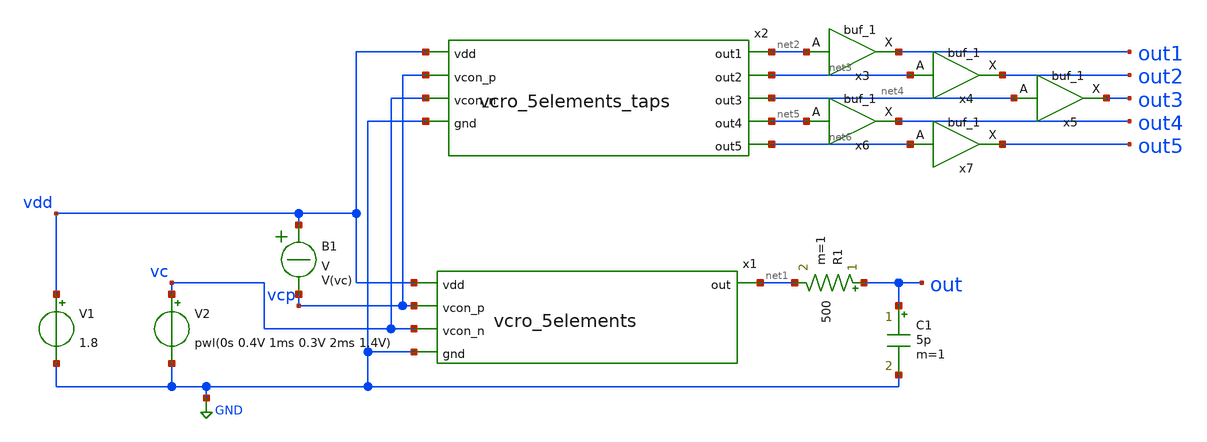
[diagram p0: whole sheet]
** sch_path: xschem/vcro_5st_tb.sch
**.subckt vcro_5st_tb
V1 vdd GND 1.8
V2 vc GND pwl(0s 0.4V 1ms 0.3V 2ms 1.4V)
R1 out net1 500 m=1
B1 vdd vcp V = V(vc)
x1 net1 vdd vcp vc GND vcro_5elements
C1 out GND 5p m=1
x2 net2 net3 net4 net5 net6 vdd vcp vc GND vcro_5elements_taps
x3 net2 GND GND vdd vdd out1 sky130_fd_sc_hd__buf_1
x4 net3 GND GND vdd vdd out2 sky130_fd_sc_hd__buf_1
x5 net4 GND GND vdd vdd out3 sky130_fd_sc_hd__buf_1
x6 net5 GND GND vdd vdd out4 sky130_fd_sc_hd__buf_1
x7 net6 GND GND vdd vdd out5 sky130_fd_sc_hd__buf_1
**** begin user architecture code
 .lib $::SKYWATER_MODELS/sky130.lib.spice tt
.include $::SKYWATER_STDCELLS/../../sky130_fd_sc_hd/spice/sky130_fd_sc_hd.spice

.param mc_mm_switch=0
.param mc_pr_switch=1



.option wnflag=0
.option savecurrents
.control
save all
tran 10n 2m 1m
plot vc vcp out
plot i(V1)
plot out1 out2 out3 out4 out5
write vcro5.raw
op
.endc


**** end user architecture code
**.ends
.GLOBAL GND
.end
